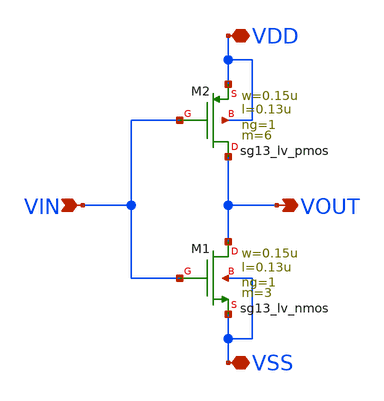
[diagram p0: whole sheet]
** sch_path: ADC8711-main/schematic/xschem/INV_D3.sch
**.subckt INV_D3 VDD VSS VOUT VIN
*.iopin VDD
*.iopin VSS
*.opin VOUT
*.ipin VIN
XM1 VOUT VIN VSS VSS sg13_lv_nmos w=0.15u l=0.13u ng=1 m=3 mm_ok=1
XM2 VOUT VIN VDD VDD sg13_lv_pmos w=0.15u l=0.13u ng=1 m=6 mm_ok=1
**.ends
.end
